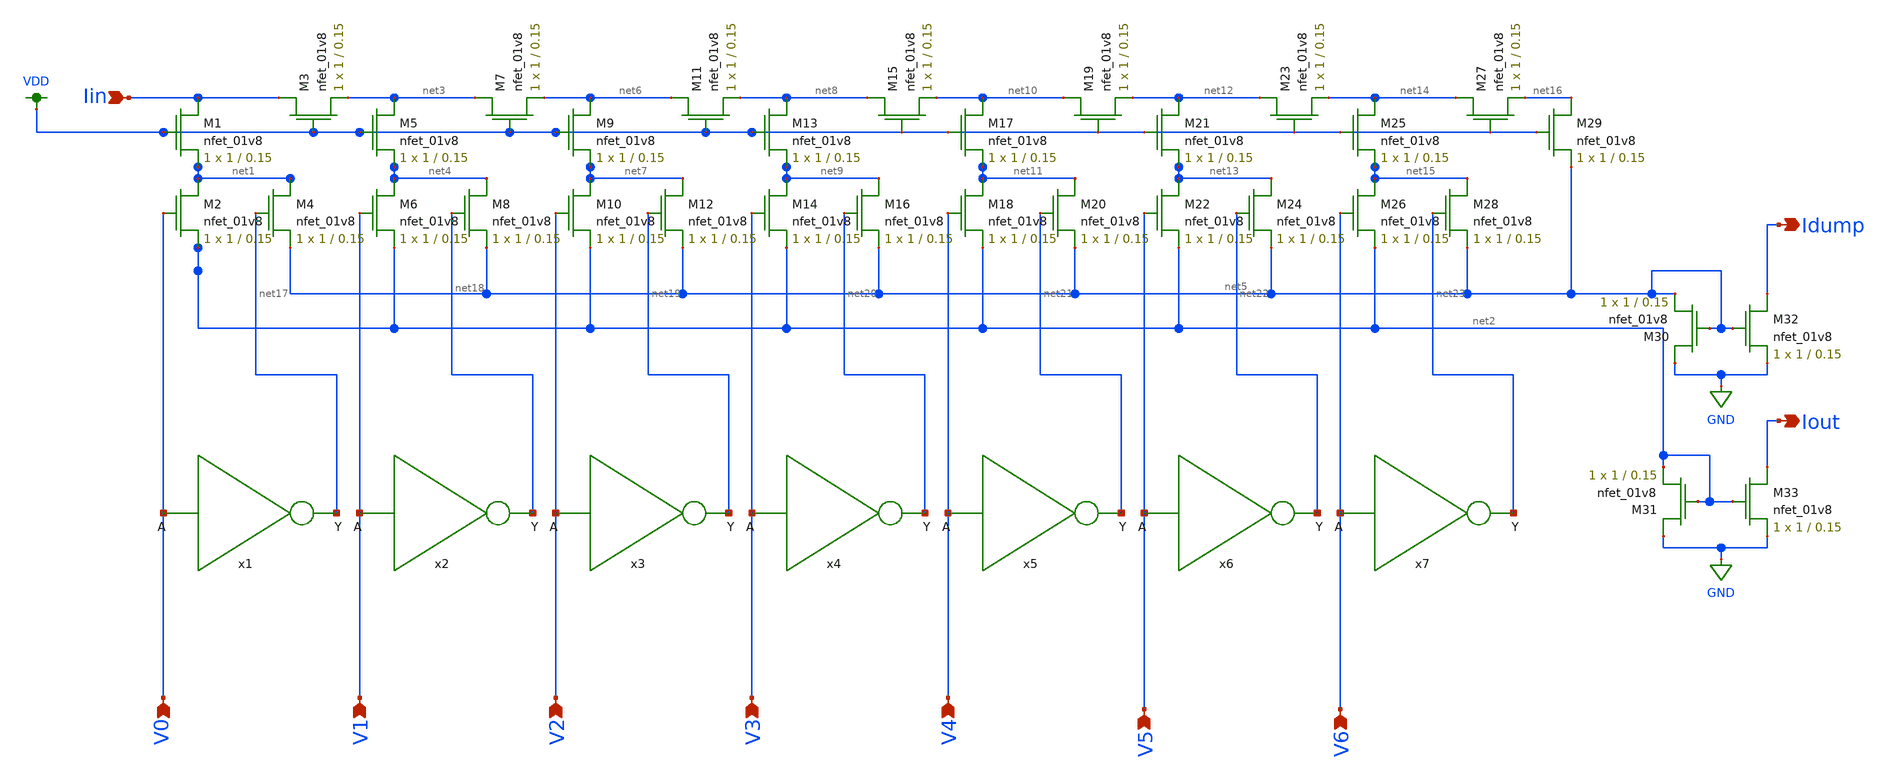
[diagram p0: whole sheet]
** sch_path: xschem/ladder.sch
**.subckt ladder Iin V0 V1 V2 V3 V4 V5 V6 Idump Iout
*.ipin Iin
*.ipin V0
*.ipin V1
*.ipin V2
*.ipin V3
*.ipin V4
*.ipin V5
*.ipin V6
*.opin Idump
*.opin Iout
XM1 Iin VDD net1 GND sky130_fd_pr__nfet_01v8 L=0.15 W=1 nf=1 ad='int((nf+1)/2) * W/nf * 0.29' as='int((nf+2)/2) * W/nf * 0.29'
+ pd='2*int((nf+1)/2) * (W/nf + 0.29)' ps='2*int((nf+2)/2) * (W/nf + 0.29)' nrd='0.29 / W' nrs='0.29 / W'
+ sa=0 sb=0 sd=0 mult=1 m=1
XM3 Iin VDD net3 GND sky130_fd_pr__nfet_01v8 L=0.15 W=1 nf=1 ad='int((nf+1)/2) * W/nf * 0.29' as='int((nf+2)/2) * W/nf * 0.29'
+ pd='2*int((nf+1)/2) * (W/nf + 0.29)' ps='2*int((nf+2)/2) * (W/nf + 0.29)' nrd='0.29 / W' nrs='0.29 / W'
+ sa=0 sb=0 sd=0 mult=1 m=1
XM5 net3 VDD net4 GND sky130_fd_pr__nfet_01v8 L=0.15 W=1 nf=1 ad='int((nf+1)/2) * W/nf * 0.29' as='int((nf+2)/2) * W/nf * 0.29'
+ pd='2*int((nf+1)/2) * (W/nf + 0.29)' ps='2*int((nf+2)/2) * (W/nf + 0.29)' nrd='0.29 / W' nrs='0.29 / W'
+ sa=0 sb=0 sd=0 mult=1 m=1
XM7 net3 VDD net6 GND sky130_fd_pr__nfet_01v8 L=0.15 W=1 nf=1 ad='int((nf+1)/2) * W/nf * 0.29' as='int((nf+2)/2) * W/nf * 0.29'
+ pd='2*int((nf+1)/2) * (W/nf + 0.29)' ps='2*int((nf+2)/2) * (W/nf + 0.29)' nrd='0.29 / W' nrs='0.29 / W'
+ sa=0 sb=0 sd=0 mult=1 m=1
XM6 net4 V1 net2 GND sky130_fd_pr__nfet_01v8 L=0.15 W=1 nf=1 ad='int((nf+1)/2) * W/nf * 0.29' as='int((nf+2)/2) * W/nf * 0.29'
+ pd='2*int((nf+1)/2) * (W/nf + 0.29)' ps='2*int((nf+2)/2) * (W/nf + 0.29)' nrd='0.29 / W' nrs='0.29 / W'
+ sa=0 sb=0 sd=0 mult=1 m=1
XM8 net4 net18 net5 GND sky130_fd_pr__nfet_01v8 L=0.15 W=1 nf=1 ad='int((nf+1)/2) * W/nf * 0.29' as='int((nf+2)/2) * W/nf * 0.29'
+ pd='2*int((nf+1)/2) * (W/nf + 0.29)' ps='2*int((nf+2)/2) * (W/nf + 0.29)' nrd='0.29 / W' nrs='0.29 / W'
+ sa=0 sb=0 sd=0 mult=1 m=1
XM2 net1 V0 net2 GND sky130_fd_pr__nfet_01v8 L=0.15 W=1 nf=1 ad='int((nf+1)/2) * W/nf * 0.29' as='int((nf+2)/2) * W/nf * 0.29'
+ pd='2*int((nf+1)/2) * (W/nf + 0.29)' ps='2*int((nf+2)/2) * (W/nf + 0.29)' nrd='0.29 / W' nrs='0.29 / W'
+ sa=0 sb=0 sd=0 mult=1 m=1
XM4 net1 net17 net5 GND sky130_fd_pr__nfet_01v8 L=0.15 W=1 nf=1 ad='int((nf+1)/2) * W/nf * 0.29' as='int((nf+2)/2) * W/nf * 0.29'
+ pd='2*int((nf+1)/2) * (W/nf + 0.29)' ps='2*int((nf+2)/2) * (W/nf + 0.29)' nrd='0.29 / W' nrs='0.29 / W'
+ sa=0 sb=0 sd=0 mult=1 m=1
XM9 net6 VDD net7 GND sky130_fd_pr__nfet_01v8 L=0.15 W=1 nf=1 ad='int((nf+1)/2) * W/nf * 0.29' as='int((nf+2)/2) * W/nf * 0.29'
+ pd='2*int((nf+1)/2) * (W/nf + 0.29)' ps='2*int((nf+2)/2) * (W/nf + 0.29)' nrd='0.29 / W' nrs='0.29 / W'
+ sa=0 sb=0 sd=0 mult=1 m=1
XM11 net6 VDD net8 GND sky130_fd_pr__nfet_01v8 L=0.15 W=1 nf=1 ad='int((nf+1)/2) * W/nf * 0.29' as='int((nf+2)/2) * W/nf * 0.29'
+ pd='2*int((nf+1)/2) * (W/nf + 0.29)' ps='2*int((nf+2)/2) * (W/nf + 0.29)' nrd='0.29 / W' nrs='0.29 / W'
+ sa=0 sb=0 sd=0 mult=1 m=1
XM10 net7 V2 net2 GND sky130_fd_pr__nfet_01v8 L=0.15 W=1 nf=1 ad='int((nf+1)/2) * W/nf * 0.29' as='int((nf+2)/2) * W/nf * 0.29'
+ pd='2*int((nf+1)/2) * (W/nf + 0.29)' ps='2*int((nf+2)/2) * (W/nf + 0.29)' nrd='0.29 / W' nrs='0.29 / W'
+ sa=0 sb=0 sd=0 mult=1 m=1
XM12 net7 net19 net5 GND sky130_fd_pr__nfet_01v8 L=0.15 W=1 nf=1 ad='int((nf+1)/2) * W/nf * 0.29' as='int((nf+2)/2) * W/nf * 0.29'
+ pd='2*int((nf+1)/2) * (W/nf + 0.29)' ps='2*int((nf+2)/2) * (W/nf + 0.29)' nrd='0.29 / W' nrs='0.29 / W'
+ sa=0 sb=0 sd=0 mult=1 m=1
XM13 net8 VDD net9 GND sky130_fd_pr__nfet_01v8 L=0.15 W=1 nf=1 ad='int((nf+1)/2) * W/nf * 0.29' as='int((nf+2)/2) * W/nf * 0.29'
+ pd='2*int((nf+1)/2) * (W/nf + 0.29)' ps='2*int((nf+2)/2) * (W/nf + 0.29)' nrd='0.29 / W' nrs='0.29 / W'
+ sa=0 sb=0 sd=0 mult=1 m=1
XM15 net8 VDD net10 GND sky130_fd_pr__nfet_01v8 L=0.15 W=1 nf=1 ad='int((nf+1)/2) * W/nf * 0.29' as='int((nf+2)/2) * W/nf * 0.29'
+ pd='2*int((nf+1)/2) * (W/nf + 0.29)' ps='2*int((nf+2)/2) * (W/nf + 0.29)' nrd='0.29 / W' nrs='0.29 / W'
+ sa=0 sb=0 sd=0 mult=1 m=1
XM14 net9 V3 net2 GND sky130_fd_pr__nfet_01v8 L=0.15 W=1 nf=1 ad='int((nf+1)/2) * W/nf * 0.29' as='int((nf+2)/2) * W/nf * 0.29'
+ pd='2*int((nf+1)/2) * (W/nf + 0.29)' ps='2*int((nf+2)/2) * (W/nf + 0.29)' nrd='0.29 / W' nrs='0.29 / W'
+ sa=0 sb=0 sd=0 mult=1 m=1
XM16 net9 net20 net5 GND sky130_fd_pr__nfet_01v8 L=0.15 W=1 nf=1 ad='int((nf+1)/2) * W/nf * 0.29' as='int((nf+2)/2) * W/nf * 0.29'
+ pd='2*int((nf+1)/2) * (W/nf + 0.29)' ps='2*int((nf+2)/2) * (W/nf + 0.29)' nrd='0.29 / W' nrs='0.29 / W'
+ sa=0 sb=0 sd=0 mult=1 m=1
XM17 net10 VDD net11 GND sky130_fd_pr__nfet_01v8 L=0.15 W=1 nf=1 ad='int((nf+1)/2) * W/nf * 0.29' as='int((nf+2)/2) * W/nf * 0.29'
+ pd='2*int((nf+1)/2) * (W/nf + 0.29)' ps='2*int((nf+2)/2) * (W/nf + 0.29)' nrd='0.29 / W' nrs='0.29 / W'
+ sa=0 sb=0 sd=0 mult=1 m=1
XM19 net10 VDD net12 GND sky130_fd_pr__nfet_01v8 L=0.15 W=1 nf=1 ad='int((nf+1)/2) * W/nf * 0.29' as='int((nf+2)/2) * W/nf * 0.29'
+ pd='2*int((nf+1)/2) * (W/nf + 0.29)' ps='2*int((nf+2)/2) * (W/nf + 0.29)' nrd='0.29 / W' nrs='0.29 / W'
+ sa=0 sb=0 sd=0 mult=1 m=1
XM18 net11 V4 net2 GND sky130_fd_pr__nfet_01v8 L=0.15 W=1 nf=1 ad='int((nf+1)/2) * W/nf * 0.29' as='int((nf+2)/2) * W/nf * 0.29'
+ pd='2*int((nf+1)/2) * (W/nf + 0.29)' ps='2*int((nf+2)/2) * (W/nf + 0.29)' nrd='0.29 / W' nrs='0.29 / W'
+ sa=0 sb=0 sd=0 mult=1 m=1
XM20 net11 net21 net5 GND sky130_fd_pr__nfet_01v8 L=0.15 W=1 nf=1 ad='int((nf+1)/2) * W/nf * 0.29' as='int((nf+2)/2) * W/nf * 0.29'
+ pd='2*int((nf+1)/2) * (W/nf + 0.29)' ps='2*int((nf+2)/2) * (W/nf + 0.29)' nrd='0.29 / W' nrs='0.29 / W'
+ sa=0 sb=0 sd=0 mult=1 m=1
XM21 net12 VDD net13 GND sky130_fd_pr__nfet_01v8 L=0.15 W=1 nf=1 ad='int((nf+1)/2) * W/nf * 0.29' as='int((nf+2)/2) * W/nf * 0.29'
+ pd='2*int((nf+1)/2) * (W/nf + 0.29)' ps='2*int((nf+2)/2) * (W/nf + 0.29)' nrd='0.29 / W' nrs='0.29 / W'
+ sa=0 sb=0 sd=0 mult=1 m=1
XM23 net12 VDD net14 GND sky130_fd_pr__nfet_01v8 L=0.15 W=1 nf=1 ad='int((nf+1)/2) * W/nf * 0.29' as='int((nf+2)/2) * W/nf * 0.29'
+ pd='2*int((nf+1)/2) * (W/nf + 0.29)' ps='2*int((nf+2)/2) * (W/nf + 0.29)' nrd='0.29 / W' nrs='0.29 / W'
+ sa=0 sb=0 sd=0 mult=1 m=1
XM22 net13 V5 net2 GND sky130_fd_pr__nfet_01v8 L=0.15 W=1 nf=1 ad='int((nf+1)/2) * W/nf * 0.29' as='int((nf+2)/2) * W/nf * 0.29'
+ pd='2*int((nf+1)/2) * (W/nf + 0.29)' ps='2*int((nf+2)/2) * (W/nf + 0.29)' nrd='0.29 / W' nrs='0.29 / W'
+ sa=0 sb=0 sd=0 mult=1 m=1
XM24 net13 net22 net5 GND sky130_fd_pr__nfet_01v8 L=0.15 W=1 nf=1 ad='int((nf+1)/2) * W/nf * 0.29' as='int((nf+2)/2) * W/nf * 0.29'
+ pd='2*int((nf+1)/2) * (W/nf + 0.29)' ps='2*int((nf+2)/2) * (W/nf + 0.29)' nrd='0.29 / W' nrs='0.29 / W'
+ sa=0 sb=0 sd=0 mult=1 m=1
XM25 net14 VDD net15 GND sky130_fd_pr__nfet_01v8 L=0.15 W=1 nf=1 ad='int((nf+1)/2) * W/nf * 0.29' as='int((nf+2)/2) * W/nf * 0.29'
+ pd='2*int((nf+1)/2) * (W/nf + 0.29)' ps='2*int((nf+2)/2) * (W/nf + 0.29)' nrd='0.29 / W' nrs='0.29 / W'
+ sa=0 sb=0 sd=0 mult=1 m=1
XM27 net14 VDD net16 GND sky130_fd_pr__nfet_01v8 L=0.15 W=1 nf=1 ad='int((nf+1)/2) * W/nf * 0.29' as='int((nf+2)/2) * W/nf * 0.29'
+ pd='2*int((nf+1)/2) * (W/nf + 0.29)' ps='2*int((nf+2)/2) * (W/nf + 0.29)' nrd='0.29 / W' nrs='0.29 / W'
+ sa=0 sb=0 sd=0 mult=1 m=1
XM26 net15 V6 net2 GND sky130_fd_pr__nfet_01v8 L=0.15 W=1 nf=1 ad='int((nf+1)/2) * W/nf * 0.29' as='int((nf+2)/2) * W/nf * 0.29'
+ pd='2*int((nf+1)/2) * (W/nf + 0.29)' ps='2*int((nf+2)/2) * (W/nf + 0.29)' nrd='0.29 / W' nrs='0.29 / W'
+ sa=0 sb=0 sd=0 mult=1 m=1
XM28 net15 net23 net5 GND sky130_fd_pr__nfet_01v8 L=0.15 W=1 nf=1 ad='int((nf+1)/2) * W/nf * 0.29' as='int((nf+2)/2) * W/nf * 0.29'
+ pd='2*int((nf+1)/2) * (W/nf + 0.29)' ps='2*int((nf+2)/2) * (W/nf + 0.29)' nrd='0.29 / W' nrs='0.29 / W'
+ sa=0 sb=0 sd=0 mult=1 m=1
XM29 net16 VDD net5 GND sky130_fd_pr__nfet_01v8 L=0.15 W=1 nf=1 ad='int((nf+1)/2) * W/nf * 0.29' as='int((nf+2)/2) * W/nf * 0.29'
+ pd='2*int((nf+1)/2) * (W/nf + 0.29)' ps='2*int((nf+2)/2) * (W/nf + 0.29)' nrd='0.29 / W' nrs='0.29 / W'
+ sa=0 sb=0 sd=0 mult=1 m=1
XM30 GND net5 net5 GND sky130_fd_pr__nfet_01v8 L=0.15 W=1 nf=1 ad='int((nf+1)/2) * W/nf * 0.29' as='int((nf+2)/2) * W/nf * 0.29'
+ pd='2*int((nf+1)/2) * (W/nf + 0.29)' ps='2*int((nf+2)/2) * (W/nf + 0.29)' nrd='0.29 / W' nrs='0.29 / W'
+ sa=0 sb=0 sd=0 mult=1 m=1
XM31 GND net2 net2 GND sky130_fd_pr__nfet_01v8 L=0.15 W=1 nf=1 ad='int((nf+1)/2) * W/nf * 0.29' as='int((nf+2)/2) * W/nf * 0.29'
+ pd='2*int((nf+1)/2) * (W/nf + 0.29)' ps='2*int((nf+2)/2) * (W/nf + 0.29)' nrd='0.29 / W' nrs='0.29 / W'
+ sa=0 sb=0 sd=0 mult=1 m=1
XM32 Idump net5 GND GND sky130_fd_pr__nfet_01v8 L=0.15 W=1 nf=1 ad='int((nf+1)/2) * W/nf * 0.29' as='int((nf+2)/2) * W/nf * 0.29'
+ pd='2*int((nf+1)/2) * (W/nf + 0.29)' ps='2*int((nf+2)/2) * (W/nf + 0.29)' nrd='0.29 / W' nrs='0.29 / W'
+ sa=0 sb=0 sd=0 mult=1 m=1
XM33 Iout net2 GND GND sky130_fd_pr__nfet_01v8 L=0.15 W=1 nf=1 ad='int((nf+1)/2) * W/nf * 0.29' as='int((nf+2)/2) * W/nf * 0.29'
+ pd='2*int((nf+1)/2) * (W/nf + 0.29)' ps='2*int((nf+2)/2) * (W/nf + 0.29)' nrd='0.29 / W' nrs='0.29 / W'
+ sa=0 sb=0 sd=0 mult=1 m=1
x1 net17 V0 inverter
x2 net18 V1 inverter
x3 net19 V2 inverter
x4 net20 V3 inverter
x5 net21 V4 inverter
x6 net22 V5 inverter
x7 net23 V6 inverter
**.ends

* expanding   symbol:  /home/madvlsi/DAC-VLSI/xschem/inverter.sym # of pins=2
** sym_path: xschem/inverter.sym
** sch_path: xschem/inverter.sch
.subckt inverter Y A
*.ipin A
*.opin Y
XM1 Y A VDD VDD sky130_fd_pr__pfet_01v8 L=0.15 W=1 nf=1 ad='int((nf+1)/2) * W/nf * 0.29' as='int((nf+2)/2) * W/nf * 0.29'
+ pd='2*int((nf+1)/2) * (W/nf + 0.29)' ps='2*int((nf+2)/2) * (W/nf + 0.29)' nrd='0.29 / W' nrs='0.29 / W'
+ sa=0 sb=0 sd=0 mult=1 m=1
XM2 Y A GND GND sky130_fd_pr__nfet_01v8 L=0.15 W=1 nf=1 ad='int((nf+1)/2) * W/nf * 0.29' as='int((nf+2)/2) * W/nf * 0.29'
+ pd='2*int((nf+1)/2) * (W/nf + 0.29)' ps='2*int((nf+2)/2) * (W/nf + 0.29)' nrd='0.29 / W' nrs='0.29 / W'
+ sa=0 sb=0 sd=0 mult=1 m=1
.ends

.GLOBAL VDD
.GLOBAL GND
.end
